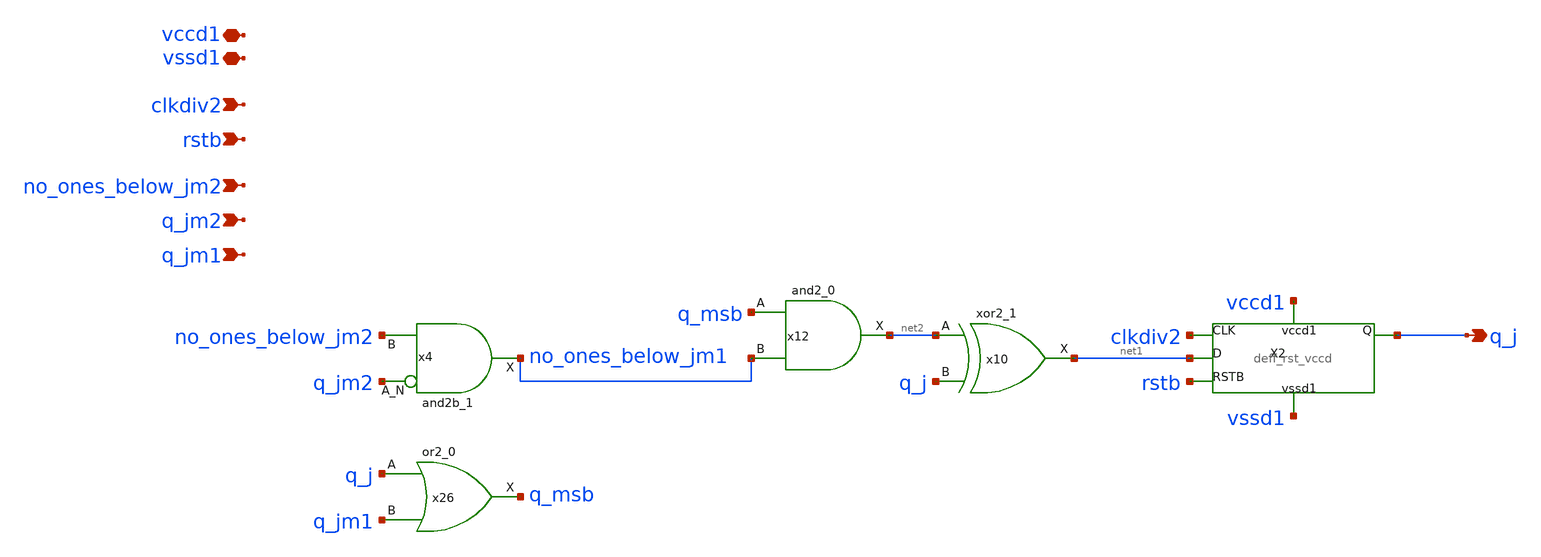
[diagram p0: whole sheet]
** sch_path: xschem/digital/gray_sine_cell.sch
**.subckt gray_sine_cell no_ones_below_jm2 q_jm2 q_jm1 vccd1 vssd1 q_j clkdiv2 rstb
*.ipin no_ones_below_jm2
*.ipin q_jm2
*.ipin q_jm1
*.iopin vccd1
*.iopin vssd1
*.opin q_j
*.ipin clkdiv2
*.ipin rstb
x4 q_jm2 no_ones_below_jm2 vssd1 vssd1 vccd1 vccd1 no_ones_below_jm1 sky130_fd_sc_hd__and2b_1
x10 net2 q_j vssd1 vssd1 vccd1 vccd1 net1 sky130_fd_sc_hd__xor2_1
x12 q_msb no_ones_below_jm1 vssd1 vssd1 vccd1 vccd1 net2 sky130_fd_sc_hd__and2_0
X2 clkdiv2 net1 q_j rstb vccd1 vssd1 deff_rst_vccd
x26 q_j q_jm1 vssd1 vssd1 vccd1 vccd1 q_msb sky130_fd_sc_hd__or2_0
**.ends

* expanding   symbol:  digital/deff_rst_vccd.sym # of pins=6
** sym_path: xschem/digital/deff_rst_vccd.sym
** sch_path: xschem/digital/deff_rst_vccd.sch
.subckt deff_rst_vccd CLK D Q RSTB vccd1 vssd1
*.ipin CLK
*.ipin D
*.opin Q
*.ipin RSTB
*.iopin vccd1
*.iopin vssd1
x3 net1 net2 net3 vssd1 vssd1 vccd1 vccd1 Q sky130_fd_sc_hd__mux2_1
x21 CLK D RSTB vssd1 vssd1 vccd1 vccd1 net1 sky130_fd_sc_hd__dfrtn_1
x1 CLK D RSTB vssd1 vssd1 vccd1 vccd1 net2 sky130_fd_sc_hd__dfrtp_1
x17 net4 vssd1 vssd1 vccd1 vccd1 net5 sky130_fd_sc_hd__buf_1
x2 net5 vssd1 vssd1 vccd1 vccd1 net3 sky130_fd_sc_hd__buf_1
x4 CLK vssd1 vssd1 vccd1 vccd1 net6 sky130_fd_sc_hd__buf_1
x5 net6 vssd1 vssd1 vccd1 vccd1 net4 sky130_fd_sc_hd__buf_1
.ends

.end
